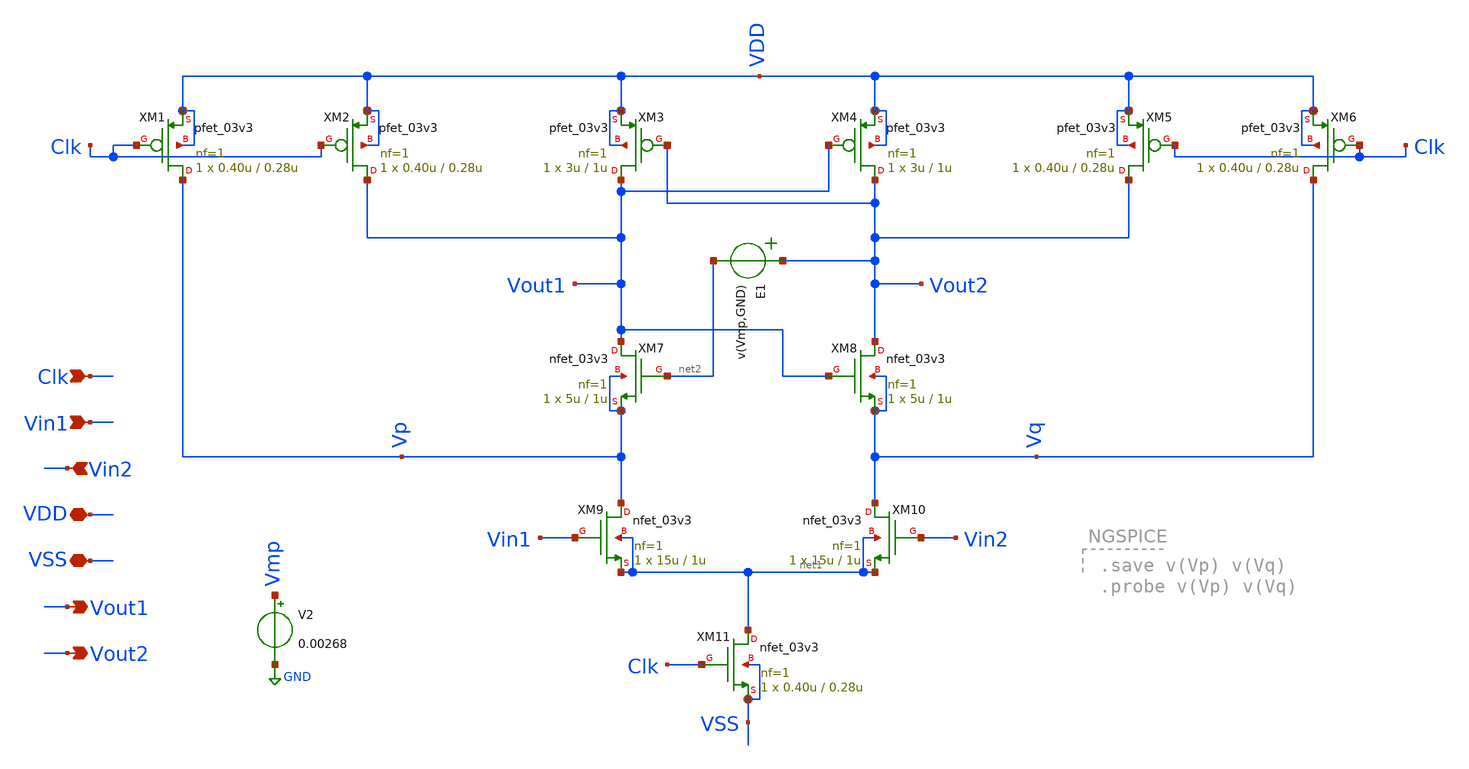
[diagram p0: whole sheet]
** sch_path: designs/comparator/strongArmLatch_offsetM7.sch
**.subckt strongArmLatch_offsetM7 Clk Vin1 Vin2 VDD VSS Vout1 Vout2
*.ipin Clk
*.ipin Vin1
*.ipin Vin2
*.iopin VDD
*.iopin VSS
*.opin Vout1
*.opin Vout2
XM1 Vp Clk VDD VDD pfet_03v3 L=0.28u W=0.40u nf=1 ad='int((nf+1)/2) * W/nf * 0.18u' as='int((nf+2)/2) * W/nf * 0.18u'
+ pd='2*int((nf+1)/2) * (W/nf + 0.18u)' ps='2*int((nf+2)/2) * (W/nf + 0.18u)' nrd='0.18u / W' nrs='0.18u / W'
+ sa=0 sb=0 sd=0 m=1
XM2 Vout1 Clk VDD VDD pfet_03v3 L=0.28u W=0.40u nf=1 ad='int((nf+1)/2) * W/nf * 0.18u' as='int((nf+2)/2) * W/nf * 0.18u'
+ pd='2*int((nf+1)/2) * (W/nf + 0.18u)' ps='2*int((nf+2)/2) * (W/nf + 0.18u)' nrd='0.18u / W' nrs='0.18u / W'
+ sa=0 sb=0 sd=0 m=1
XM3 Vout1 Vout2 VDD VDD pfet_03v3 L=1u W=3u nf=1 ad='int((nf+1)/2) * W/nf * 0.18u' as='int((nf+2)/2) * W/nf * 0.18u'
+ pd='2*int((nf+1)/2) * (W/nf + 0.18u)' ps='2*int((nf+2)/2) * (W/nf + 0.18u)' nrd='0.18u / W' nrs='0.18u / W'
+ sa=0 sb=0 sd=0 m=1
XM4 Vout2 Vout1 VDD VDD pfet_03v3 L=1u W=3u nf=1 ad='int((nf+1)/2) * W/nf * 0.18u' as='int((nf+2)/2) * W/nf * 0.18u'
+ pd='2*int((nf+1)/2) * (W/nf + 0.18u)' ps='2*int((nf+2)/2) * (W/nf + 0.18u)' nrd='0.18u / W' nrs='0.18u / W'
+ sa=0 sb=0 sd=0 m=1
XM5 Vout2 Clk VDD VDD pfet_03v3 L=0.28u W=0.40u nf=1 ad='int((nf+1)/2) * W/nf * 0.18u' as='int((nf+2)/2) * W/nf * 0.18u'
+ pd='2*int((nf+1)/2) * (W/nf + 0.18u)' ps='2*int((nf+2)/2) * (W/nf + 0.18u)' nrd='0.18u / W' nrs='0.18u / W'
+ sa=0 sb=0 sd=0 m=1
XM6 Vq Clk VDD VDD pfet_03v3 L=0.28u W=0.40u nf=1 ad='int((nf+1)/2) * W/nf * 0.18u' as='int((nf+2)/2) * W/nf * 0.18u'
+ pd='2*int((nf+1)/2) * (W/nf + 0.18u)' ps='2*int((nf+2)/2) * (W/nf + 0.18u)' nrd='0.18u / W' nrs='0.18u / W'
+ sa=0 sb=0 sd=0 m=1
XM7 Vout1 net2 Vp Vp nfet_03v3 L=1u W=5u nf=1 ad='int((nf+1)/2) * W/nf * 0.18u' as='int((nf+2)/2) * W/nf * 0.18u'
+ pd='2*int((nf+1)/2) * (W/nf + 0.18u)' ps='2*int((nf+2)/2) * (W/nf + 0.18u)' nrd='0.18u / W' nrs='0.18u / W'
+ sa=0 sb=0 sd=0 m=1
XM8 Vout2 Vout1 Vq Vq nfet_03v3 L=1u W=5u nf=1 ad='int((nf+1)/2) * W/nf * 0.18u' as='int((nf+2)/2) * W/nf * 0.18u'
+ pd='2*int((nf+1)/2) * (W/nf + 0.18u)' ps='2*int((nf+2)/2) * (W/nf + 0.18u)' nrd='0.18u / W' nrs='0.18u / W'
+ sa=0 sb=0 sd=0 m=1
XM9 Vp Vin1 net1 net1 nfet_03v3 L=1u W=15u nf=1 ad='int((nf+1)/2) * W/nf * 0.18u' as='int((nf+2)/2) * W/nf * 0.18u'
+ pd='2*int((nf+1)/2) * (W/nf + 0.18u)' ps='2*int((nf+2)/2) * (W/nf + 0.18u)' nrd='0.18u / W' nrs='0.18u / W'
+ sa=0 sb=0 sd=0 m=1
XM10 Vq Vin2 net1 net1 nfet_03v3 L=1u W=15u nf=1 ad='int((nf+1)/2) * W/nf * 0.18u' as='int((nf+2)/2) * W/nf * 0.18u'
+ pd='2*int((nf+1)/2) * (W/nf + 0.18u)' ps='2*int((nf+2)/2) * (W/nf + 0.18u)' nrd='0.18u / W' nrs='0.18u / W'
+ sa=0 sb=0 sd=0 m=1
XM11 net1 Clk VSS VSS nfet_03v3 L=0.28u W=0.40u nf=1 ad='int((nf+1)/2) * W/nf * 0.18u' as='int((nf+2)/2) * W/nf * 0.18u'
+ pd='2*int((nf+1)/2) * (W/nf + 0.18u)' ps='2*int((nf+2)/2) * (W/nf + 0.18u)' nrd='0.18u / W' nrs='0.18u / W'
+ sa=0 sb=0 sd=0 m=1
V2 Vmp GND 0.00268
E1 Vout2 net2 VOL=' v(Vmp,GND) '
**.ends
.GLOBAL GND
.end
